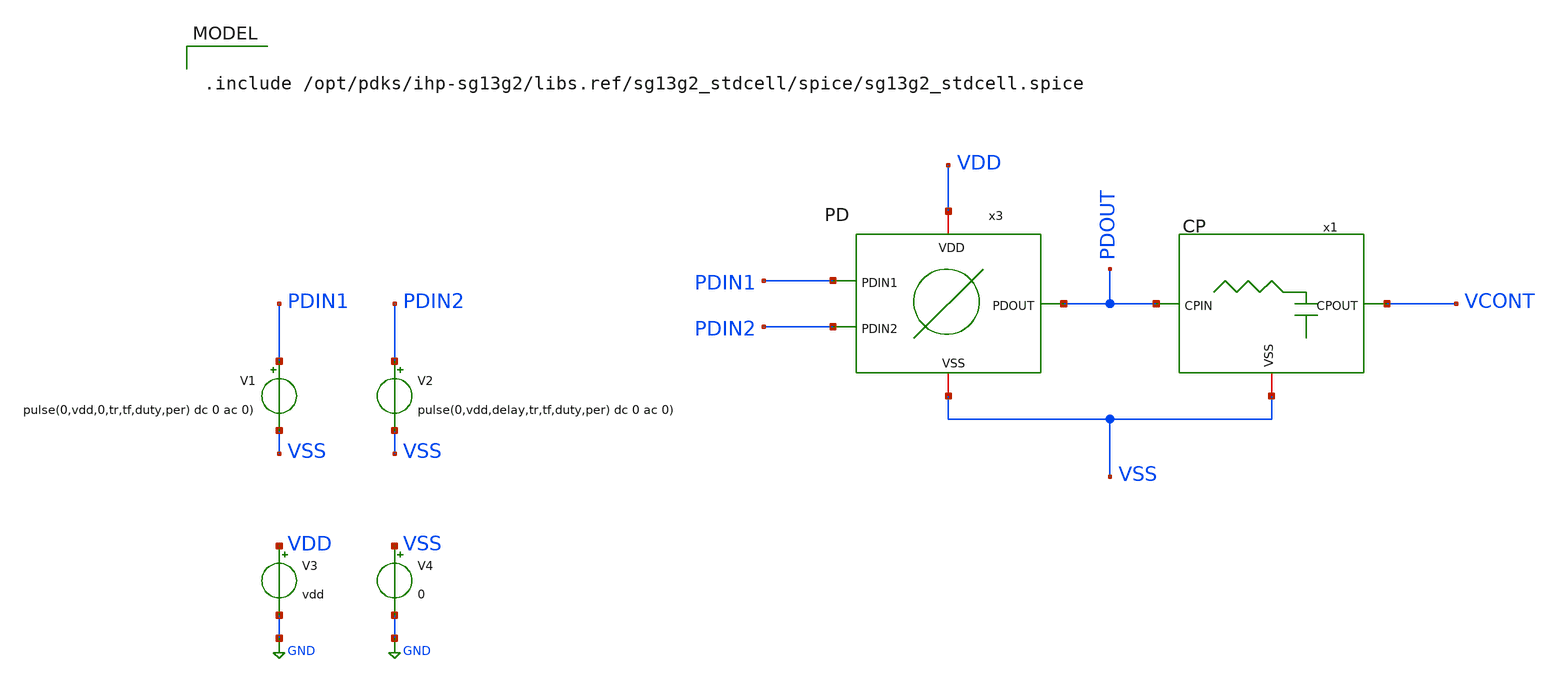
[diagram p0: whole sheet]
** sch_path: QDLL6501-main/schematic/xschem/testbenchs/tb_TB_CP.sch
**.subckt tb_TB_CP
V1 PDIN1 VSS pulse(0,vdd,0,tr,tf,duty,per) dc 0 ac 0)
V2 PDIN2 VSS pulse(0,vdd,delay,tr,tf,duty,per) dc 0 ac 0)
V3 VDD GND vdd
V4 VSS GND 0
x3 VDD VSS PDIN1 PDOUT PDIN2 PD
x1 PDOUT VCONT VSS CP
**** begin user architecture code

.include /opt/pdks/ihp-sg13g2/libs.ref/sg13g2_stdcell/spice/sg13g2_stdcell.spice



.param temp=65 vdd=1.2
.param per=4n duty=2n tr=20p tf=20p delay=2n
.param vin=1.2 vd={vdd}


.lib cornerMOSlv.lib mos_tt
.lib cornerCAP.lib cap_typ
.lib cornerRES.lib res_typ


.options method=gear reltol=1e-1 abstol=1e-1 vntol=1e-1
.control
 set color0 = white
 save all
 tran 2p 1u 0.05n
 plot v(PDIN1) v(PDIN2)
 plot v(VCONT)
 plot v(PDOUT)
.endc


**** end user architecture code
**.ends

* expanding   symbol:  IHP__MPC0349/dependencies/IHP__QDLL6501/QDLL6501-main/schematic/xschem/PD.sym
*+ # of pins=5
** sym_path: IHP__MPC0349/dependencies/IHP__QDLL6501/QDLL6501-main/schematic/xschem/PD.sym
** sch_path: IHP__MPC0349/dependencies/IHP__QDLL6501/QDLL6501-main/schematic/xschem/PD.sch
.subckt PD VDD VSS PDIN1 PDOUT PDIN2
*.iopin VDD
*.iopin VSS
*.opin PDOUT
*.ipin PDIN1
*.ipin PDIN2
x1 PDOUT PDIN1 PDIN2 VDD VSS sg13g2_xor2_1
.ends


* expanding   symbol:  IHP__MPC0349/dependencies/IHP__QDLL6501/QDLL6501-main/schematic/xschem/CP.sym
*+ # of pins=3
** sym_path: IHP__MPC0349/dependencies/IHP__QDLL6501/QDLL6501-main/schematic/xschem/CP.sym
** sch_path: IHP__MPC0349/dependencies/IHP__QDLL6501/QDLL6501-main/schematic/xschem/CP.sch
.subckt CP CPIN CPOUT VSS
*.iopin VSS
*.ipin CPIN
*.opin CPOUT
XC1 CPOUT VSS cap_cmim w=60e-6 l=20e-6 m=1 mm_ok=1
x1 CPOUT CPIN VSS RES
.ends


* expanding   symbol:  sg13g2_xor2_1.sym # of pins=3
** sym_path: sg13g2_xor2_1.sym
** sch_path: sg13g2_xor2_1.sch
.subckt sg13g2_xor2_1 X A B VDD VSS
*.opin X
*.ipin B
*.ipin A
*.iopin VDD
*.iopin VSS
XM1 net1 A VSS VSS sg13_lv_nmos w=550.00n l=130.00n ng=1 m=1 mm_ok=1
XM2 net1 B VSS VSS sg13_lv_nmos w=550.00n l=130.00n ng=1 m=1 mm_ok=1
XM3 X net1 VSS VSS sg13_lv_nmos w=740.00n l=130.00n ng=1 m=1 mm_ok=1
XM4 X B net3 VSS sg13_lv_nmos w=740.00n l=130.00n ng=1 m=1 mm_ok=1
XM5 net3 A VSS VSS sg13_lv_nmos w=740.00n l=130.00n ng=1 m=1 mm_ok=1
XM6 net4 A VDD VDD sg13_lv_pmos w=1.000u l=130.00n ng=1 m=1 mm_ok=1
XM7 net1 B net4 VDD sg13_lv_pmos w=1.000u l=130.00n ng=1 m=1 mm_ok=1
XM8 net2 A VDD VDD sg13_lv_pmos w=1.12u l=130.00n ng=1 m=1 mm_ok=1
XM9 X net1 net2 VDD sg13_lv_pmos w=1.12u l=130.00n ng=1 m=1 mm_ok=1
XM10 net2 B VDD VDD sg13_lv_pmos w=1.12u l=130.00n ng=1 m=1 mm_ok=1
.ends


* expanding   symbol:  RES.sym # of pins=3
** sym_path: QDLL6501-main/schematic/xschem/RES.sym
** sch_path: QDLL6501-main/schematic/xschem/RES.sch
.subckt RES ROUT RIN VSS
*.ipin RIN
*.opin ROUT
*.iopin VSS
XR13 net1 RIN VSS rppd w=1e-6 l=10e-6 m=1 b=0 mm_ok=1
XR1 net2 net1 VSS rppd w=1e-6 l=10e-6 m=1 b=0 mm_ok=1
XR2 net3 net2 VSS rppd w=1e-6 l=10e-6 m=1 b=0 mm_ok=1
XR3 net4 net3 VSS rppd w=1e-6 l=10e-6 m=1 b=0 mm_ok=1
XR4 net5 net4 VSS rppd w=1e-6 l=10e-6 m=1 b=0 mm_ok=1
XR5 net6 net5 VSS rppd w=1e-6 l=10e-6 m=1 b=0 mm_ok=1
XR6 net7 net6 VSS rppd w=1e-6 l=10e-6 m=1 b=0 mm_ok=1
XR7 net8 net7 VSS rppd w=1e-6 l=10e-6 m=1 b=0 mm_ok=1
XR8 net9 net8 VSS rppd w=1e-6 l=10e-6 m=1 b=0 mm_ok=1
XR9 net10 net9 VSS rppd w=1e-6 l=10e-6 m=1 b=0 mm_ok=1
XR10 net11 net10 VSS rppd w=1e-6 l=10e-6 m=1 b=0 mm_ok=1
XR11 ROUT net11 VSS rppd w=1e-6 l=10e-6 m=1 b=0 mm_ok=1
.ends

.GLOBAL GND
.end
